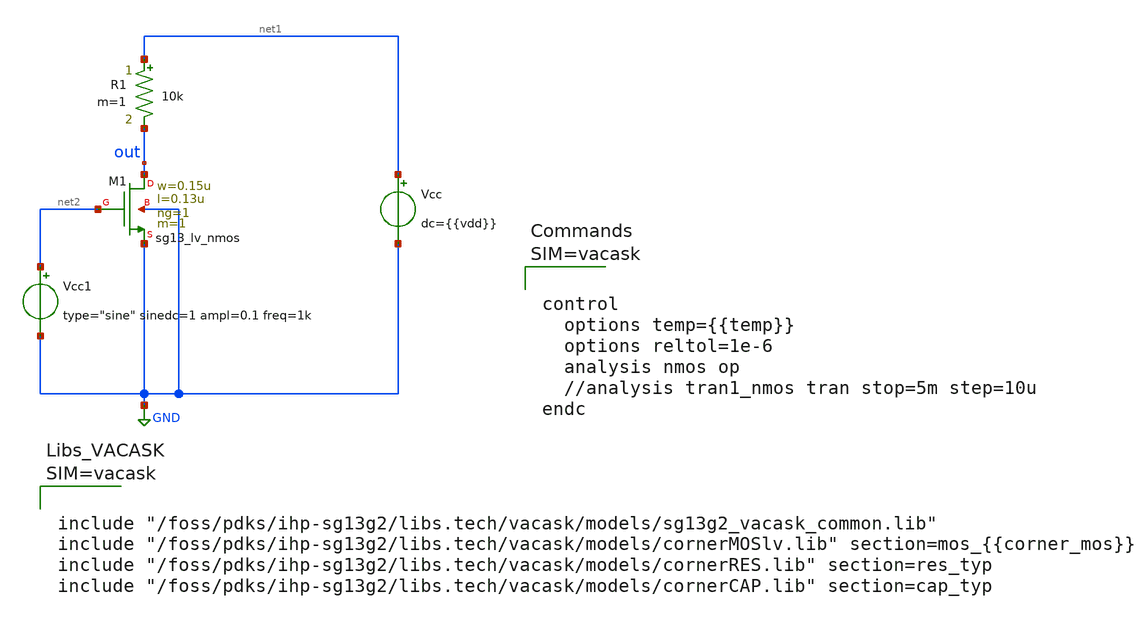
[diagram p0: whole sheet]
** sch_path: examples/source_follower/tb/nmos.sch
**.subckt nmos
R1 net1 out 10k m=1
Vcc net1 GND dc={{vdd}}
XM1 out net2 GND GND sg13_lv_nmos w=0.15u l=0.13u ng=1 m=1 mm_ok=1
Vcc1 net2 GND type="sine" sinedc=1 ampl=0.1 freq=1k
**** begin user architecture code






**** end user architecture code
**.ends
.GLOBAL GND
.end
